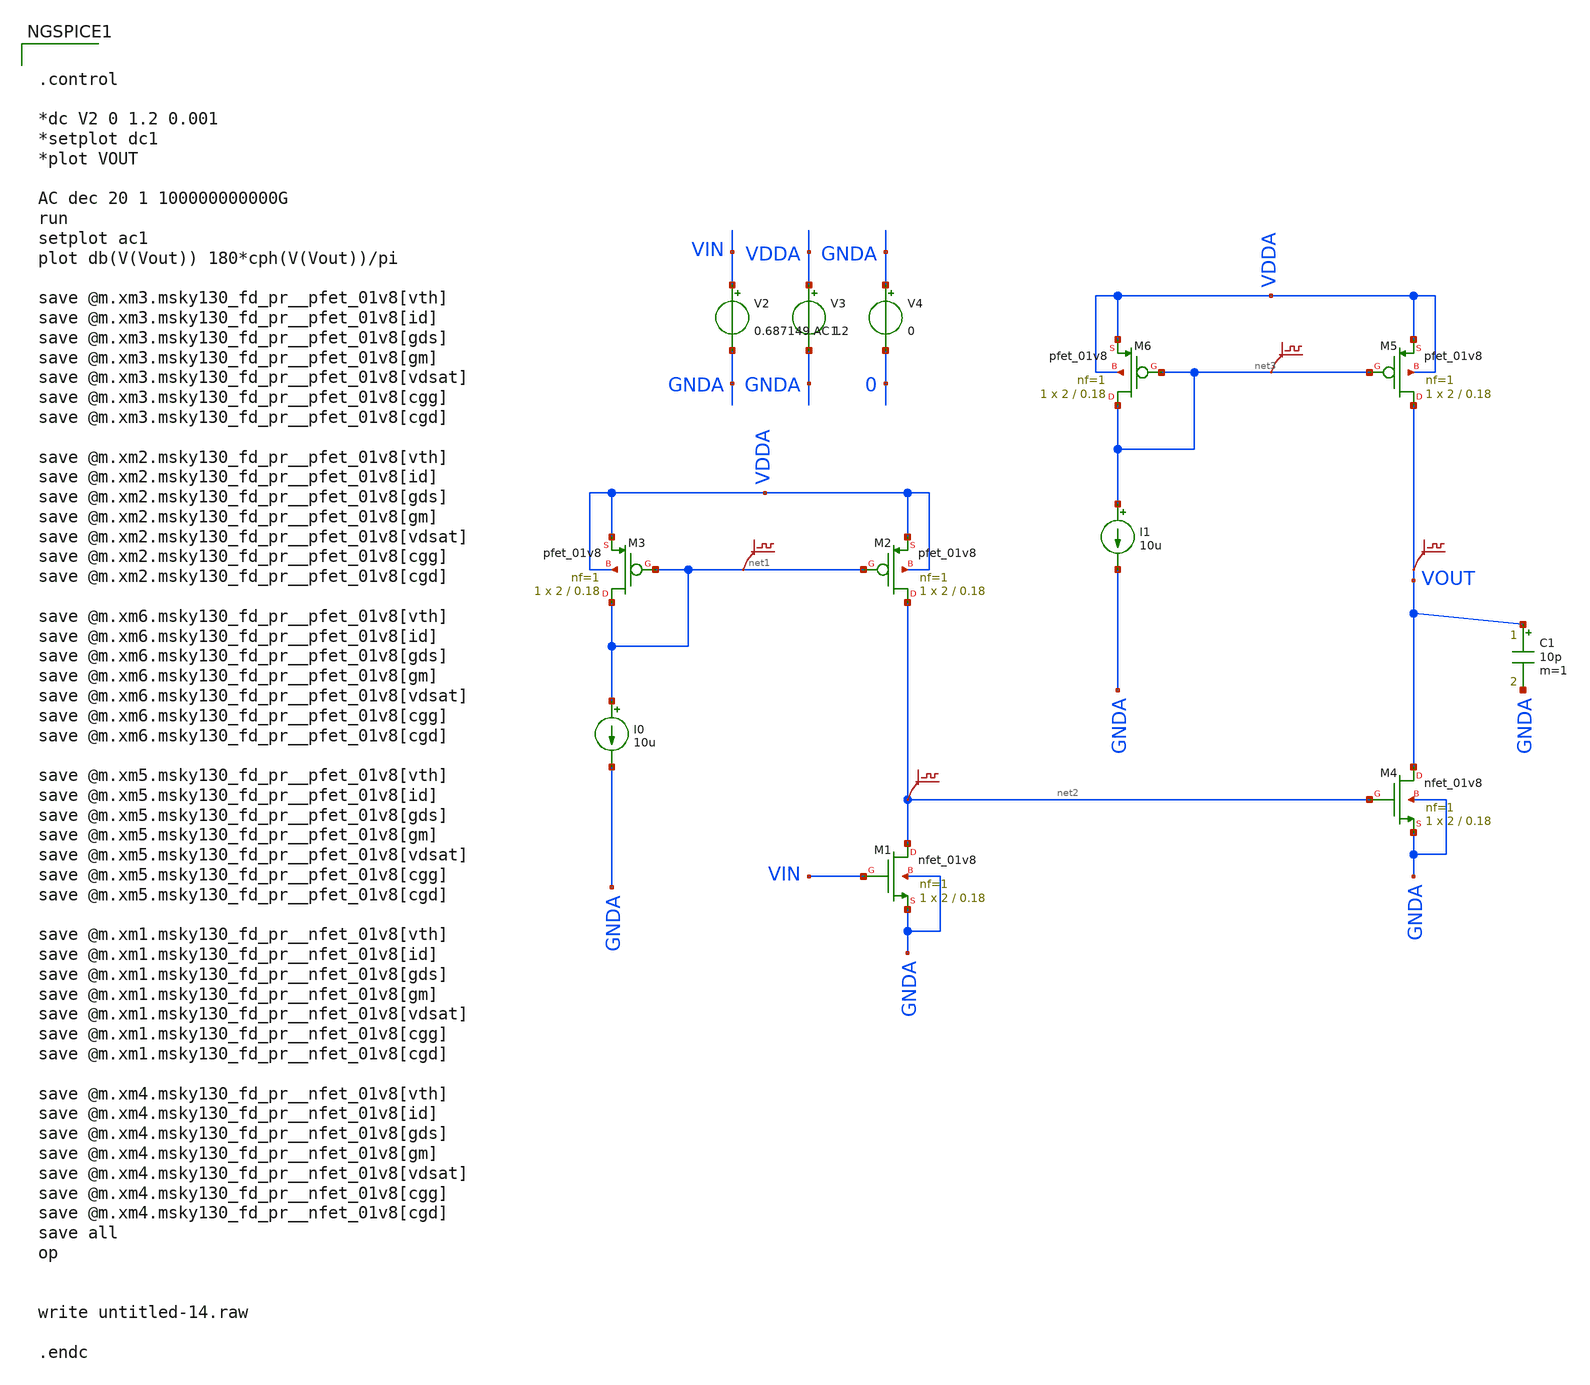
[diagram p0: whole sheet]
** sch_path: untitled-14.sch
**.subckt untitled-14
XM1 net2 VIN GNDA GNDA sky130_fd_pr__nfet_01v8 L=0.18 W=2 nf=1 ad='int((nf+1)/2) * W/nf * 0.29' as='int((nf+2)/2) * W/nf * 0.29'
+ pd='2*int((nf+1)/2) * (W/nf + 0.29)' ps='2*int((nf+2)/2) * (W/nf + 0.29)' nrd='0.29 / W' nrs='0.29 / W'
+ sa=0 sb=0 sd=0 mult=1 m=1
XM2 net2 net1 VDDA VDDA sky130_fd_pr__pfet_01v8 L=0.18 W=2 nf=1 ad='int((nf+1)/2) * W/nf * 0.29' as='int((nf+2)/2) * W/nf * 0.29'
+ pd='2*int((nf+1)/2) * (W/nf + 0.29)' ps='2*int((nf+2)/2) * (W/nf + 0.29)' nrd='0.29 / W' nrs='0.29 / W'
+ sa=0 sb=0 sd=0 mult=1 m=1
XM3 net1 net1 VDDA VDDA sky130_fd_pr__pfet_01v8 L=0.18 W=2 nf=1 ad='int((nf+1)/2) * W/nf * 0.29' as='int((nf+2)/2) * W/nf * 0.29'
+ pd='2*int((nf+1)/2) * (W/nf + 0.29)' ps='2*int((nf+2)/2) * (W/nf + 0.29)' nrd='0.29 / W' nrs='0.29 / W'
+ sa=0 sb=0 sd=0 mult=1 m=1
I0 net1 GNDA 10u
XM4 VOUT net2 GNDA GNDA sky130_fd_pr__nfet_01v8 L=0.18 W=2 nf=1 ad='int((nf+1)/2) * W/nf * 0.29' as='int((nf+2)/2) * W/nf * 0.29'
+ pd='2*int((nf+1)/2) * (W/nf + 0.29)' ps='2*int((nf+2)/2) * (W/nf + 0.29)' nrd='0.29 / W' nrs='0.29 / W'
+ sa=0 sb=0 sd=0 mult=1 m=1
XM5 VOUT net3 VDDA VDDA sky130_fd_pr__pfet_01v8 L=0.18 W=2 nf=1 ad='int((nf+1)/2) * W/nf * 0.29' as='int((nf+2)/2) * W/nf * 0.29'
+ pd='2*int((nf+1)/2) * (W/nf + 0.29)' ps='2*int((nf+2)/2) * (W/nf + 0.29)' nrd='0.29 / W' nrs='0.29 / W'
+ sa=0 sb=0 sd=0 mult=1 m=1
XM6 net3 net3 VDDA VDDA sky130_fd_pr__pfet_01v8 L=0.18 W=2 nf=1 ad='int((nf+1)/2) * W/nf * 0.29' as='int((nf+2)/2) * W/nf * 0.29'
+ pd='2*int((nf+1)/2) * (W/nf + 0.29)' ps='2*int((nf+2)/2) * (W/nf + 0.29)' nrd='0.29 / W' nrs='0.29 / W'
+ sa=0 sb=0 sd=0 mult=1 m=1
I1 net3 GNDA 10u
V2 VIN GNDA 0.687149 AC 1
V3 VDDA GNDA 1.2
V4 GNDA 0 0
.save v(net2)
.save v(net1)
.save v(net3)
.save v(vout)
C1 VOUT GNDA 10p m=1
**** begin user architecture code

** opencircuitdesign pdks install
.lib $::SKYWATER_MODELS/sky130.lib.spice tt




.control

*dc V2 0 1.2 0.001
*setplot dc1
*plot VOUT

AC dec 20 1 100000000000G
run
setplot ac1
plot db(V(Vout)) 180*cph(V(Vout))/pi

save @m.xm3.msky130_fd_pr__pfet_01v8[vth]
save @m.xm3.msky130_fd_pr__pfet_01v8[id]
save @m.xm3.msky130_fd_pr__pfet_01v8[gds]
save @m.xm3.msky130_fd_pr__pfet_01v8[gm]
save @m.xm3.msky130_fd_pr__pfet_01v8[vdsat]
save @m.xm3.msky130_fd_pr__pfet_01v8[cgg]
save @m.xm3.msky130_fd_pr__pfet_01v8[cgd]

save @m.xm2.msky130_fd_pr__pfet_01v8[vth]
save @m.xm2.msky130_fd_pr__pfet_01v8[id]
save @m.xm2.msky130_fd_pr__pfet_01v8[gds]
save @m.xm2.msky130_fd_pr__pfet_01v8[gm]
save @m.xm2.msky130_fd_pr__pfet_01v8[vdsat]
save @m.xm2.msky130_fd_pr__pfet_01v8[cgg]
save @m.xm2.msky130_fd_pr__pfet_01v8[cgd]

save @m.xm6.msky130_fd_pr__pfet_01v8[vth]
save @m.xm6.msky130_fd_pr__pfet_01v8[id]
save @m.xm6.msky130_fd_pr__pfet_01v8[gds]
save @m.xm6.msky130_fd_pr__pfet_01v8[gm]
save @m.xm6.msky130_fd_pr__pfet_01v8[vdsat]
save @m.xm6.msky130_fd_pr__pfet_01v8[cgg]
save @m.xm6.msky130_fd_pr__pfet_01v8[cgd]

save @m.xm5.msky130_fd_pr__pfet_01v8[vth]
save @m.xm5.msky130_fd_pr__pfet_01v8[id]
save @m.xm5.msky130_fd_pr__pfet_01v8[gds]
save @m.xm5.msky130_fd_pr__pfet_01v8[gm]
save @m.xm5.msky130_fd_pr__pfet_01v8[vdsat]
save @m.xm5.msky130_fd_pr__pfet_01v8[cgg]
save @m.xm5.msky130_fd_pr__pfet_01v8[cgd]

save @m.xm1.msky130_fd_pr__nfet_01v8[vth]
save @m.xm1.msky130_fd_pr__nfet_01v8[id]
save @m.xm1.msky130_fd_pr__nfet_01v8[gds]
save @m.xm1.msky130_fd_pr__nfet_01v8[gm]
save @m.xm1.msky130_fd_pr__nfet_01v8[vdsat]
save @m.xm1.msky130_fd_pr__nfet_01v8[cgg]
save @m.xm1.msky130_fd_pr__nfet_01v8[cgd]

save @m.xm4.msky130_fd_pr__nfet_01v8[vth]
save @m.xm4.msky130_fd_pr__nfet_01v8[id]
save @m.xm4.msky130_fd_pr__nfet_01v8[gds]
save @m.xm4.msky130_fd_pr__nfet_01v8[gm]
save @m.xm4.msky130_fd_pr__nfet_01v8[vdsat]
save @m.xm4.msky130_fd_pr__nfet_01v8[cgg]
save @m.xm4.msky130_fd_pr__nfet_01v8[cgd]
save all
op


write untitled-14.raw

.endc


**** end user architecture code
**.ends
.end
